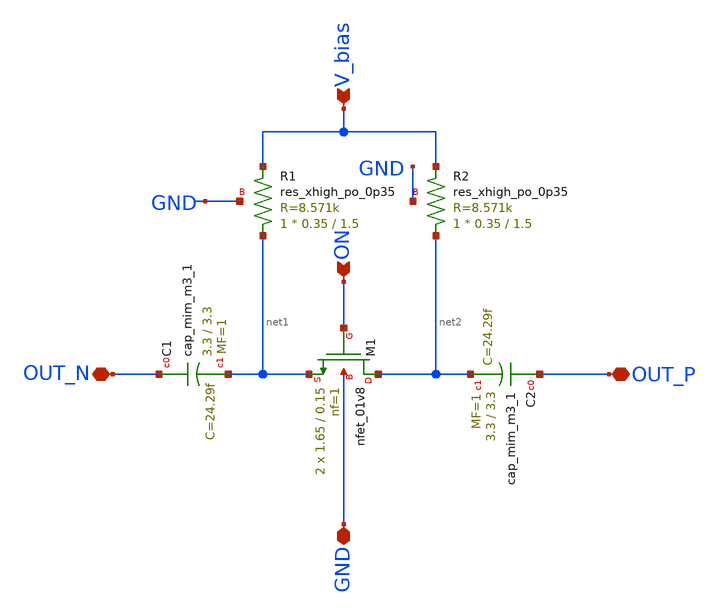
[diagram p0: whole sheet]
** sch_path: xschem/cell_unit.sch
**.subckt cell_unit OUT_N OUT_P GND ON V_bias
*.iopin OUT_N
*.iopin OUT_P
*.iopin GND
*.ipin ON
*.ipin V_bias
XC1 OUT_N net1 sky130_fd_pr__cap_mim_m3_1 W=3.3 L=3.3 MF=1 m=1
XC2 OUT_P net2 sky130_fd_pr__cap_mim_m3_1 W=3.3 L=3.3 MF=1 m=1
XM1 net2 ON net1 GND sky130_fd_pr__nfet_01v8 L=0.15 W=1.65 nf=1 ad='int((nf+1)/2) * W/nf * 0.29' as='int((nf+2)/2) * W/nf * 0.29'
+ pd='2*int((nf+1)/2) * (W/nf + 0.29)' ps='2*int((nf+2)/2) * (W/nf + 0.29)' nrd='0.29 / W' nrs='0.29 / W'
+ sa=0 sb=0 sd=0 mult=2 m=2
XR1 net1 V_bias GND sky130_fd_pr__res_xhigh_po_0p35 L=1.5 mult=1 m=1
XR2 net2 V_bias GND sky130_fd_pr__res_xhigh_po_0p35 L=1.5 mult=1 m=1
**.ends
.end
